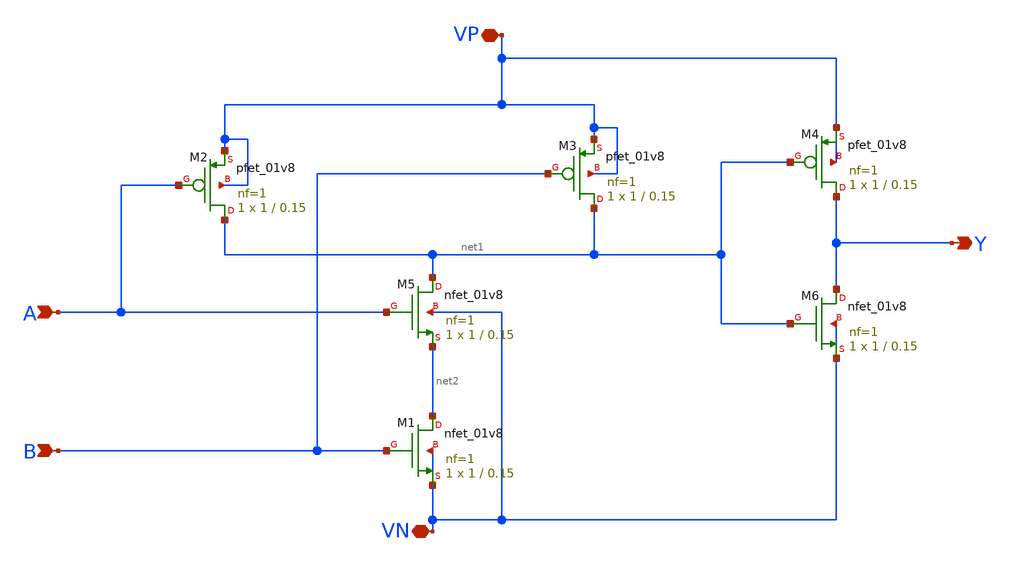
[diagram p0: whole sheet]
** sch_path: and.sch
**.subckt and Y VP VN A B
*.opin Y
*.iopin VP
*.iopin VN
*.ipin A
*.ipin B
XM5 net1 A net2 VN sky130_fd_pr__nfet_01v8 L=0.15 W=1 nf=1 ad='int((nf+1)/2) * W/nf * 0.29' as='int((nf+2)/2) * W/nf * 0.29'
+ pd='2*int((nf+1)/2) * (W/nf + 0.29)' ps='2*int((nf+2)/2) * (W/nf + 0.29)' nrd='0.29 / W' nrs='0.29 / W'
+ sa=0 sb=0 sd=0 mult=1 m=1
XM1 net2 B VN VN sky130_fd_pr__nfet_01v8 L=0.15 W=1 nf=1 ad='int((nf+1)/2) * W/nf * 0.29' as='int((nf+2)/2) * W/nf * 0.29'
+ pd='2*int((nf+1)/2) * (W/nf + 0.29)' ps='2*int((nf+2)/2) * (W/nf + 0.29)' nrd='0.29 / W' nrs='0.29 / W'
+ sa=0 sb=0 sd=0 mult=1 m=1
XM2 net1 A VP VP sky130_fd_pr__pfet_01v8 L=0.15 W=1 nf=1 ad='int((nf+1)/2) * W/nf * 0.29' as='int((nf+2)/2) * W/nf * 0.29'
+ pd='2*int((nf+1)/2) * (W/nf + 0.29)' ps='2*int((nf+2)/2) * (W/nf + 0.29)' nrd='0.29 / W' nrs='0.29 / W'
+ sa=0 sb=0 sd=0 mult=1 m=1
XM3 net1 B VP VP sky130_fd_pr__pfet_01v8 L=0.15 W=1 nf=1 ad='int((nf+1)/2) * W/nf * 0.29' as='int((nf+2)/2) * W/nf * 0.29'
+ pd='2*int((nf+1)/2) * (W/nf + 0.29)' ps='2*int((nf+2)/2) * (W/nf + 0.29)' nrd='0.29 / W' nrs='0.29 / W'
+ sa=0 sb=0 sd=0 mult=1 m=1
XM4 Y net1 VP VP sky130_fd_pr__pfet_01v8 L=0.15 W=1 nf=1 ad='int((nf+1)/2) * W/nf * 0.29' as='int((nf+2)/2) * W/nf * 0.29'
+ pd='2*int((nf+1)/2) * (W/nf + 0.29)' ps='2*int((nf+2)/2) * (W/nf + 0.29)' nrd='0.29 / W' nrs='0.29 / W'
+ sa=0 sb=0 sd=0 mult=1 m=1
XM6 Y net1 VN VN sky130_fd_pr__nfet_01v8 L=0.15 W=1 nf=1 ad='int((nf+1)/2) * W/nf * 0.29' as='int((nf+2)/2) * W/nf * 0.29'
+ pd='2*int((nf+1)/2) * (W/nf + 0.29)' ps='2*int((nf+2)/2) * (W/nf + 0.29)' nrd='0.29 / W' nrs='0.29 / W'
+ sa=0 sb=0 sd=0 mult=1 m=1
**.ends
.end
